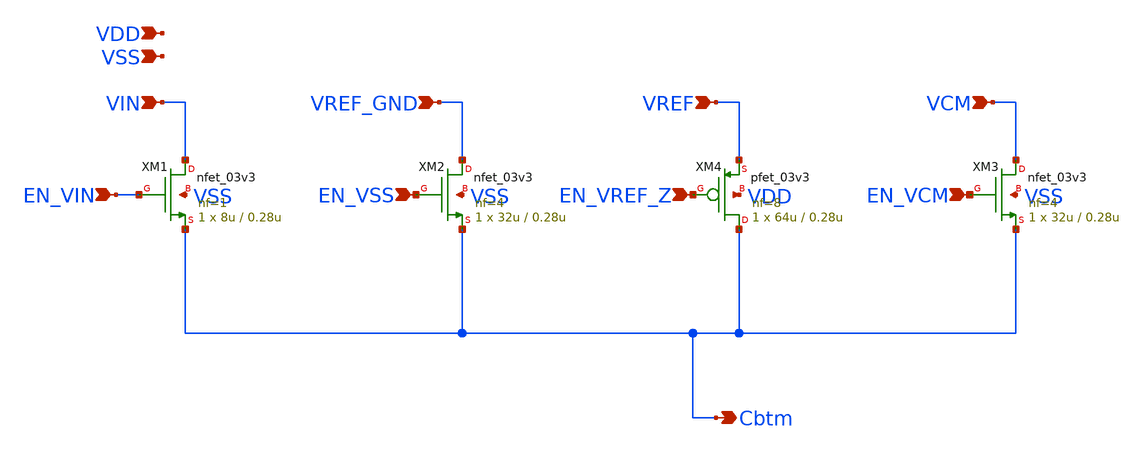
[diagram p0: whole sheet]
** sch_path: Schematic/individual_switch/swtich_C8.sch
**.subckt swtich_C8 VIN EN_VIN VREF_GND VREF VCM EN_VCM Cbtm VDD EN_VSS EN_VREF_Z VSS
*.ipin VIN
*.ipin EN_VIN
*.ipin VREF_GND
*.ipin VREF
*.ipin VCM
*.ipin EN_VCM
*.opin Cbtm
*.ipin VDD
*.ipin EN_VSS
*.ipin EN_VREF_Z
*.ipin VSS
XM1 VIN EN_VIN Cbtm VSS nfet_03v3 L=0.28u W=8u nf=1 ad='int((nf+1)/2) * W/nf * 0.18u' as='int((nf+2)/2) * W/nf * 0.18u'
+ pd='2*int((nf+1)/2) * (W/nf + 0.18u)' ps='2*int((nf+2)/2) * (W/nf + 0.18u)' nrd='0.18u / W' nrs='0.18u / W'
+ sa=0 sb=0 sd=0 m=1
XM2 VREF_GND EN_VSS Cbtm VSS nfet_03v3 L=0.28u W=32u nf=4 ad='int((nf+1)/2) * W/nf * 0.18u' as='int((nf+2)/2) * W/nf * 0.18u'
+ pd='2*int((nf+1)/2) * (W/nf + 0.18u)' ps='2*int((nf+2)/2) * (W/nf + 0.18u)' nrd='0.18u / W' nrs='0.18u / W'
+ sa=0 sb=0 sd=0 m=1
XM3 VCM EN_VCM Cbtm VSS nfet_03v3 L=0.28u W=32u nf=4 ad='int((nf+1)/2) * W/nf * 0.18u' as='int((nf+2)/2) * W/nf * 0.18u'
+ pd='2*int((nf+1)/2) * (W/nf + 0.18u)' ps='2*int((nf+2)/2) * (W/nf + 0.18u)' nrd='0.18u / W' nrs='0.18u / W'
+ sa=0 sb=0 sd=0 m=1
XM4 Cbtm EN_VREF_Z VREF VDD pfet_03v3 L=0.28u W=64u nf=8 ad='int((nf+1)/2) * W/nf * 0.18u' as='int((nf+2)/2) * W/nf * 0.18u'
+ pd='2*int((nf+1)/2) * (W/nf + 0.18u)' ps='2*int((nf+2)/2) * (W/nf + 0.18u)' nrd='0.18u / W' nrs='0.18u / W'
+ sa=0 sb=0 sd=0 m=1
**.ends
.end
